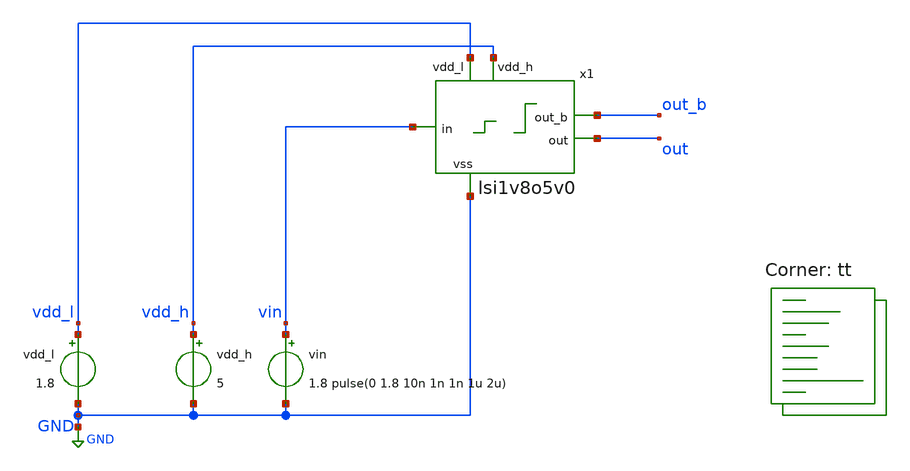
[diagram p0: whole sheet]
** sch_path: xschem/test_lsi1v8o5v0.sch
**.subckt test_lsi1v8o5v0
x1 vin out_b out vdd_l vdd_h GND lsi1v8o5v0
vdd_l vdd_l GND 1.8
vin vin GND 1.8 pulse(0 1.8 10n 1n 1n 1u 2u)
vdd_h vdd_h GND 5
**** begin user architecture code
.lib $::SKYWATER_MODELS/sky130.lib.spice tt



.include 'lsi1v8o5v0.spice'
.options savecurrents
.control
  save all
  op
  remzerovec
  write test_lsi1v8o5v0.raw
  set appendwrite
  * tran
  tran 1n 3u
  remzerovec
  write test_lsi1v8o5v0.raw
.endc



**** end user architecture code
**.ends
.GLOBAL GND
.end
